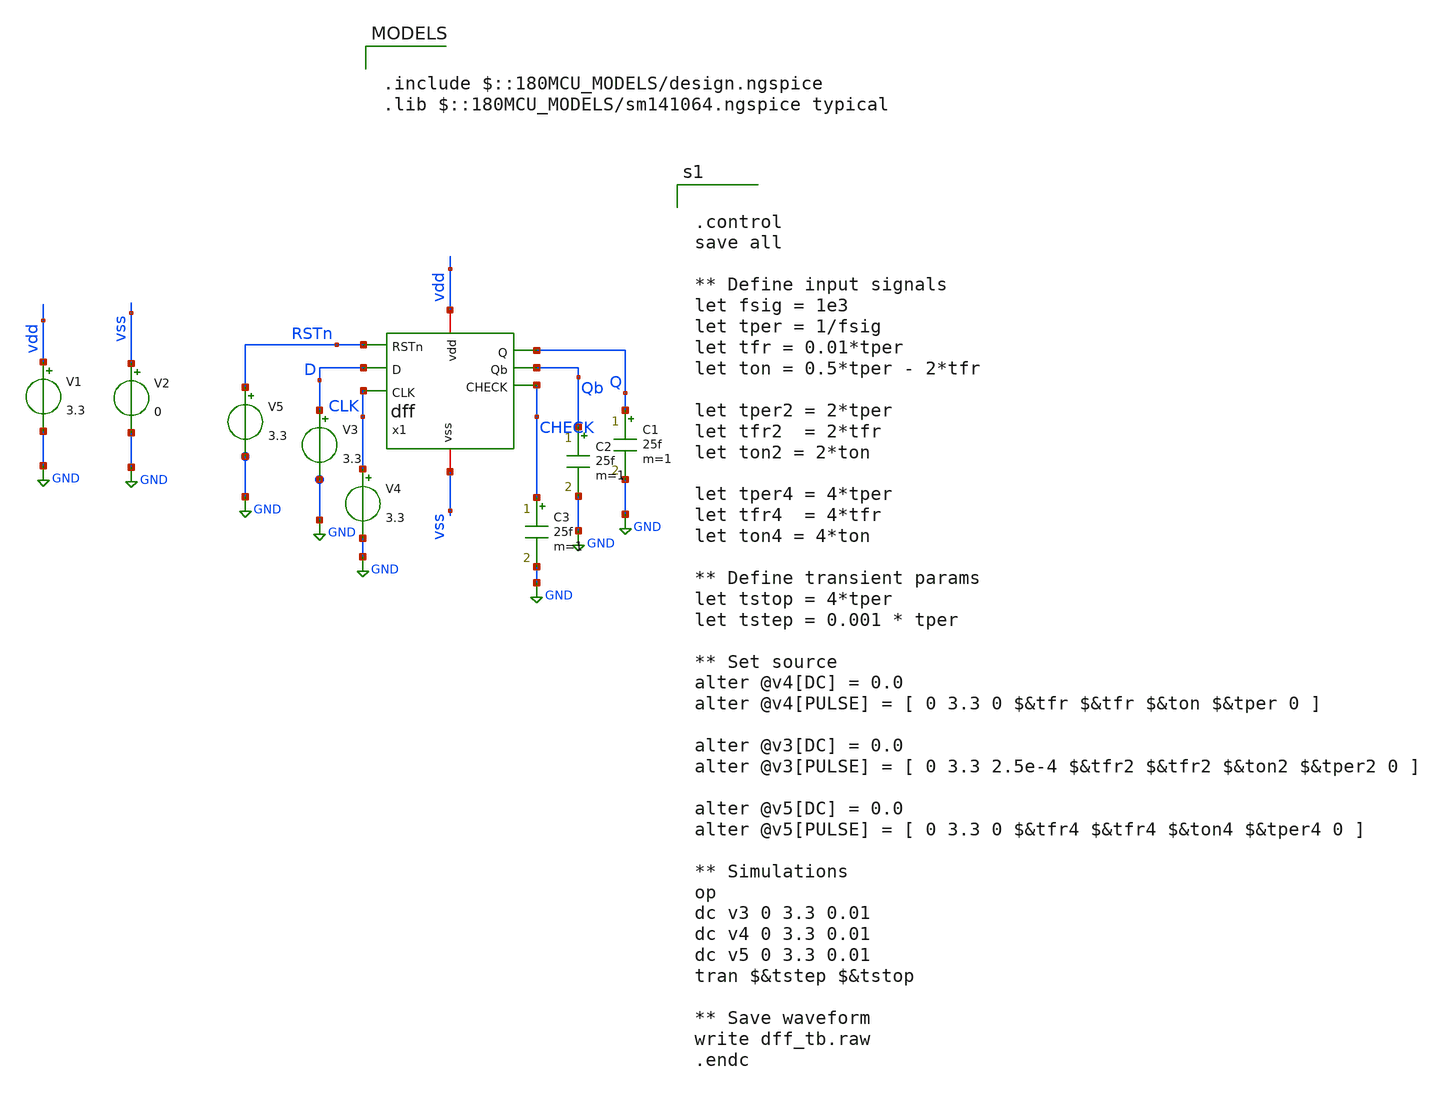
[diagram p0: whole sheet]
** sch_path: dff_tb.sch
**.subckt dff_tb
V1 vdd GND 3.3
V2 vss GND 0
V3 D GND 3.3
C1 Q GND 25f m=1
V4 CLK GND 3.3
C2 Qb GND 25f m=1
V5 RSTn GND 3.3
x1 RSTn vdd D Q CHECK vss Qb CLK dff
C3 CHECK GND 25f m=1
**** begin user architecture code

.include $::180MCU_MODELS/design.ngspice
.lib $::180MCU_MODELS/sm141064.ngspice typical



.control
save all

** Define input signals
let fsig = 1e3
let tper = 1/fsig
let tfr = 0.01*tper
let ton = 0.5*tper - 2*tfr

let tper2 = 2*tper
let tfr2  = 2*tfr
let ton2 = 2*ton

let tper4 = 4*tper
let tfr4  = 4*tfr
let ton4 = 4*ton

** Define transient params
let tstop = 4*tper
let tstep = 0.001 * tper

** Set source
alter @v4[DC] = 0.0
alter @v4[PULSE] = [ 0 3.3 0 $&tfr $&tfr $&ton $&tper 0 ]

alter @v3[DC] = 0.0
alter @v3[PULSE] = [ 0 3.3 2.5e-4 $&tfr2 $&tfr2 $&ton2 $&tper2 0 ]

alter @v5[DC] = 0.0
alter @v5[PULSE] = [ 0 3.3 0 $&tfr4 $&tfr4 $&ton4 $&tper4 0 ]

** Simulations
op
dc v3 0 3.3 0.01
dc v4 0 3.3 0.01
dc v5 0 3.3 0.01
tran $&tstep $&tstop

** Save waveform
write dff_tb.raw
.endc


**** end user architecture code
**.ends

* expanding   symbol:  dff.sym # of pins=8
** sym_path: dff.sym
** sch_path: dff.sch
.subckt dff RSTn vdd D Q CHECK vss Qb CLK
*.ipin CLK
*.ipin RSTn
*.opin Qb
*.opin Q
*.ipin D
*.iopin vdd
*.iopin vss
*.opin CHECK
x1 CHECK vdd cbar c vss net1 tgate
x4 vdd net1 net2 RSTn vss nand2
x3 vdd CHECK net2 vss inv
x5 net2 vdd cbar c vss net5 tgate
x6 vdd net3 net5 RSTn vss nand2
x7 vdd c net5 net3 cbar vss tristate
x8 vdd net3 Q vss inv
x9 vdd net3 net4 vss inv
x10 vdd net4 Qb vss inv
x11 vdd CLK cbar vss inv
x12 vdd cbar c vss inv
x13 vdd c CHECK D cbar vss tristate
.ends


* expanding   symbol:  tgate.sym # of pins=6
** sym_path: tgate.sym
** sch_path: tgate.sch
.subckt tgate in vdd cbar c vss out
*.ipin in
*.opin out
*.ipin cbar
*.ipin c
*.iopin vdd
*.iopin vss
XM1 out cbar in vdd pfet_03v3 L=0.28u W=0.42u nf=1 ad='int((nf+1)/2) * W/nf * 0.18u' as='int((nf+2)/2) * W/nf * 0.18u'
+ pd='2*int((nf+1)/2) * (W/nf + 0.18u)' ps='2*int((nf+2)/2) * (W/nf + 0.18u)' nrd='0.18u / W' nrs='0.18u / W'
+ sa=0 sb=0 sd=0 m=1
XM2 out c in vss nfet_03v3 L=0.28u W=0.42u nf=1 ad='int((nf+1)/2) * W/nf * 0.18u' as='int((nf+2)/2) * W/nf * 0.18u'
+ pd='2*int((nf+1)/2) * (W/nf + 0.18u)' ps='2*int((nf+2)/2) * (W/nf + 0.18u)' nrd='0.18u / W' nrs='0.18u / W'
+ sa=0 sb=0 sd=0 m=1
.ends


* expanding   symbol:  nand2.sym # of pins=5
** sym_path: nand2.sym
** sch_path: nand2.sch
.subckt nand2 vdd OUT IN0 IN1 vss
*.ipin IN0
*.ipin IN1
*.opin OUT
*.iopin vdd
*.iopin vss
XM1 net1 IN1 vss vss nfet_03v3 L=0.28u W=1u nf=1 ad='int((nf+1)/2) * W/nf * 0.18u' as='int((nf+2)/2) * W/nf * 0.18u'
+ pd='2*int((nf+1)/2) * (W/nf + 0.18u)' ps='2*int((nf+2)/2) * (W/nf + 0.18u)' nrd='0.18u / W' nrs='0.18u / W'
+ sa=0 sb=0 sd=0 m=1
XM3 OUT IN0 vdd vdd pfet_03v3 L=0.28u W=1u nf=1 ad='int((nf+1)/2) * W/nf * 0.18u' as='int((nf+2)/2) * W/nf * 0.18u'
+ pd='2*int((nf+1)/2) * (W/nf + 0.18u)' ps='2*int((nf+2)/2) * (W/nf + 0.18u)' nrd='0.18u / W' nrs='0.18u / W'
+ sa=0 sb=0 sd=0 m=1
XM4 OUT IN1 vdd vdd pfet_03v3 L=0.28u W=1u nf=1 ad='int((nf+1)/2) * W/nf * 0.18u' as='int((nf+2)/2) * W/nf * 0.18u'
+ pd='2*int((nf+1)/2) * (W/nf + 0.18u)' ps='2*int((nf+2)/2) * (W/nf + 0.18u)' nrd='0.18u / W' nrs='0.18u / W'
+ sa=0 sb=0 sd=0 m=1
XM2 OUT IN0 net1 vss nfet_03v3 L=0.28u W=1u nf=1 ad='int((nf+1)/2) * W/nf * 0.18u' as='int((nf+2)/2) * W/nf * 0.18u'
+ pd='2*int((nf+1)/2) * (W/nf + 0.18u)' ps='2*int((nf+2)/2) * (W/nf + 0.18u)' nrd='0.18u / W' nrs='0.18u / W'
+ sa=0 sb=0 sd=0 m=1
.ends


* expanding   symbol:  inv.sym # of pins=4
** sym_path: inv.sym
** sch_path: inv.sch
.subckt inv vdd IN OUT vss
*.ipin IN
*.opin OUT
*.iopin vdd
*.iopin vss
XM1 OUT IN vss vss nfet_03v3 L=0.28u W=1u nf=1 ad='int((nf+1)/2) * W/nf * 0.18u' as='int((nf+2)/2) * W/nf * 0.18u'
+ pd='2*int((nf+1)/2) * (W/nf + 0.18u)' ps='2*int((nf+2)/2) * (W/nf + 0.18u)' nrd='0.18u / W' nrs='0.18u / W'
+ sa=0 sb=0 sd=0 m=1
XM2 OUT IN vdd vdd pfet_03v3 L=0.28u W=1u nf=1 ad='int((nf+1)/2) * W/nf * 0.18u' as='int((nf+2)/2) * W/nf * 0.18u'
+ pd='2*int((nf+1)/2) * (W/nf + 0.18u)' ps='2*int((nf+2)/2) * (W/nf + 0.18u)' nrd='0.18u / W' nrs='0.18u / W'
+ sa=0 sb=0 sd=0 m=1
.ends


* expanding   symbol:  tristate.sym # of pins=6
** sym_path: tristate.sym
** sch_path: tristate.sch
.subckt tristate vdd c out in cbar vss
*.ipin in
*.opin out
*.iopin vdd
*.iopin vss
*.ipin c
*.ipin cbar
XM1 net1 c vdd vdd pfet_03v3 L=0.28u W=0.42u nf=1 ad='int((nf+1)/2) * W/nf * 0.18u' as='int((nf+2)/2) * W/nf * 0.18u'
+ pd='2*int((nf+1)/2) * (W/nf + 0.18u)' ps='2*int((nf+2)/2) * (W/nf + 0.18u)' nrd='0.18u / W' nrs='0.18u / W'
+ sa=0 sb=0 sd=0 m=1
XM2 out in net1 vdd pfet_03v3 L=0.28u W=0.42u nf=1 ad='int((nf+1)/2) * W/nf * 0.18u' as='int((nf+2)/2) * W/nf * 0.18u'
+ pd='2*int((nf+1)/2) * (W/nf + 0.18u)' ps='2*int((nf+2)/2) * (W/nf + 0.18u)' nrd='0.18u / W' nrs='0.18u / W'
+ sa=0 sb=0 sd=0 m=1
XM3 out in net2 vss nfet_03v3 L=0.28u W=0.42u nf=1 ad='int((nf+1)/2) * W/nf * 0.18u' as='int((nf+2)/2) * W/nf * 0.18u'
+ pd='2*int((nf+1)/2) * (W/nf + 0.18u)' ps='2*int((nf+2)/2) * (W/nf + 0.18u)' nrd='0.18u / W' nrs='0.18u / W'
+ sa=0 sb=0 sd=0 m=1
XM4 net2 cbar vss vss nfet_03v3 L=0.28u W=0.42u nf=1 ad='int((nf+1)/2) * W/nf * 0.18u' as='int((nf+2)/2) * W/nf * 0.18u'
+ pd='2*int((nf+1)/2) * (W/nf + 0.18u)' ps='2*int((nf+2)/2) * (W/nf + 0.18u)' nrd='0.18u / W' nrs='0.18u / W'
+ sa=0 sb=0 sd=0 m=1
.ends

.GLOBAL GND
.end
